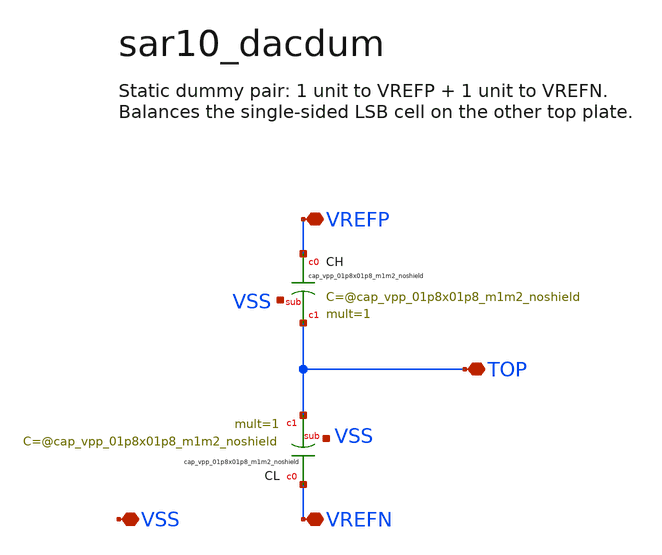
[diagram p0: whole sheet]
** sch_path: xschem/sar10_dacdum.sch
**.subckt sar10_dacdum TOP VREFP VREFN VSS
*.iopin TOP
*.iopin VREFP
*.iopin VREFN
*.iopin VSS
XCH VREFP TOP VSS sky130_fd_pr__cap_vpp_01p8x01p8_m1m2_noshield mult=1 m=1
XCL VREFN TOP VSS sky130_fd_pr__cap_vpp_01p8x01p8_m1m2_noshield mult=1 m=1
**.ends
.end
